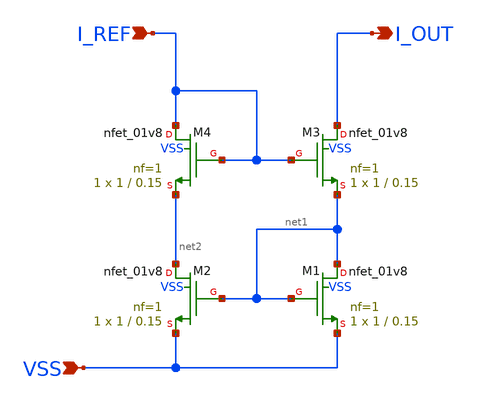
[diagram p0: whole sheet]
** sch_path: designs/analog_library/bias_4.sch
**.subckt bias_4 I_REF I_OUT VSS
*.ipin I_REF
*.opin I_OUT
*.ipin VSS
XM1 net1 net1 VSS VSS sky130_fd_pr__nfet_01v8 L=0.15 W=1 nf=1 ad='int((nf+1)/2) * W/nf * 0.29' as='int((nf+2)/2) * W/nf * 0.29'
+ pd='2*int((nf+1)/2) * (W/nf + 0.29)' ps='2*int((nf+2)/2) * (W/nf + 0.29)' nrd='0.29 / W' nrs='0.29 / W'
+ sa=0 sb=0 sd=0 mult=1 m=1
XM2 net2 net1 VSS VSS sky130_fd_pr__nfet_01v8 L=0.15 W=1 nf=1 ad='int((nf+1)/2) * W/nf * 0.29' as='int((nf+2)/2) * W/nf * 0.29'
+ pd='2*int((nf+1)/2) * (W/nf + 0.29)' ps='2*int((nf+2)/2) * (W/nf + 0.29)' nrd='0.29 / W' nrs='0.29 / W'
+ sa=0 sb=0 sd=0 mult=1 m=1
XM3 I_OUT I_REF net1 VSS sky130_fd_pr__nfet_01v8 L=0.15 W=1 nf=1 ad='int((nf+1)/2) * W/nf * 0.29' as='int((nf+2)/2) * W/nf * 0.29'
+ pd='2*int((nf+1)/2) * (W/nf + 0.29)' ps='2*int((nf+2)/2) * (W/nf + 0.29)' nrd='0.29 / W' nrs='0.29 / W'
+ sa=0 sb=0 sd=0 mult=1 m=1
XM4 I_REF I_REF net2 VSS sky130_fd_pr__nfet_01v8 L=0.15 W=1 nf=1 ad='int((nf+1)/2) * W/nf * 0.29' as='int((nf+2)/2) * W/nf * 0.29'
+ pd='2*int((nf+1)/2) * (W/nf + 0.29)' ps='2*int((nf+2)/2) * (W/nf + 0.29)' nrd='0.29 / W' nrs='0.29 / W'
+ sa=0 sb=0 sd=0 mult=1 m=1
**.ends
.end
